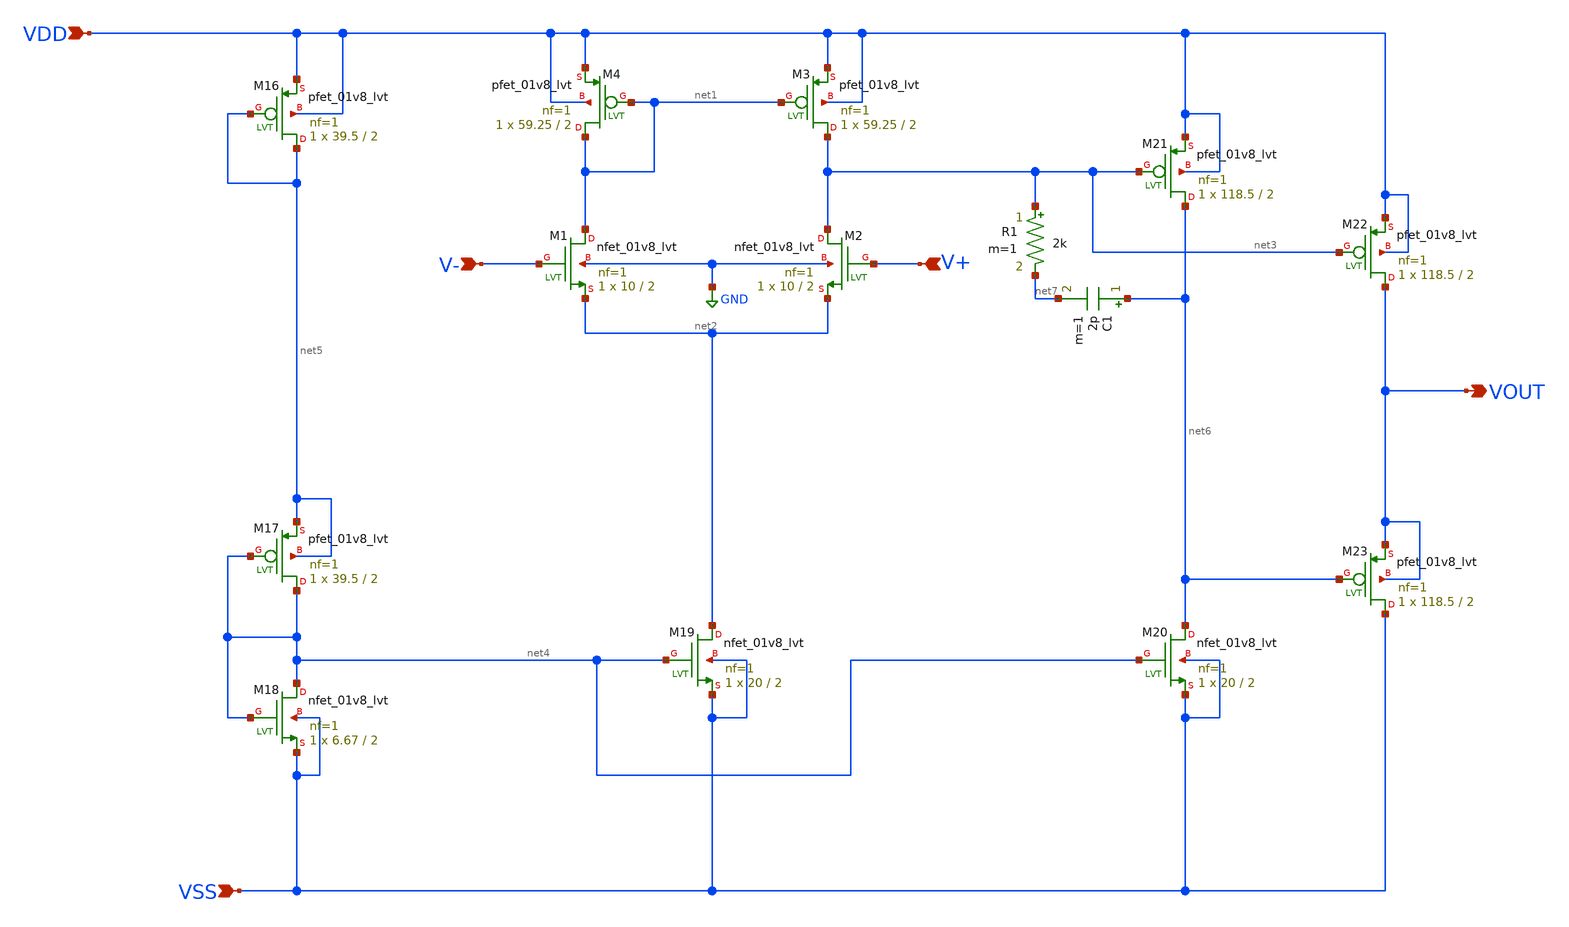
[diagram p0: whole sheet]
** sch_path: OPA.sch
**.subckt OPA VSS VOUT VDD V- V+
*.ipin VSS
*.opin VOUT
*.ipin VDD
*.ipin V-
*.ipin V+
XM16 net5 net5 VDD VDD sky130_fd_pr__pfet_01v8_lvt L=2 W=39.5 nf=1 ad='int((nf+1)/2) * W/nf * 0.29' as='int((nf+2)/2) * W/nf * 0.29'
+ pd='2*int((nf+1)/2) * (W/nf + 0.29)' ps='2*int((nf+2)/2) * (W/nf + 0.29)' nrd='0.29 / W' nrs='0.29 / W'
+ sa=0 sb=0 sd=0 mult=1 m=1
XM17 net4 net4 net5 net5 sky130_fd_pr__pfet_01v8_lvt L=2 W=39.5 nf=1 ad='int((nf+1)/2) * W/nf * 0.29'
+ as='int((nf+2)/2) * W/nf * 0.29' pd='2*int((nf+1)/2) * (W/nf + 0.29)' ps='2*int((nf+2)/2) * (W/nf + 0.29)'
+ nrd='0.29 / W' nrs='0.29 / W' sa=0 sb=0 sd=0 mult=1 m=1
XM18 net4 net4 VSS VSS sky130_fd_pr__nfet_01v8_lvt L=2 W=6.67 nf=1 ad='int((nf+1)/2) * W/nf * 0.29' as='int((nf+2)/2) * W/nf * 0.29'
+ pd='2*int((nf+1)/2) * (W/nf + 0.29)' ps='2*int((nf+2)/2) * (W/nf + 0.29)' nrd='0.29 / W' nrs='0.29 / W'
+ sa=0 sb=0 sd=0 mult=1 m=1
XM19 net2 net4 VSS VSS sky130_fd_pr__nfet_01v8_lvt L=2 W=20 nf=1 ad='int((nf+1)/2) * W/nf * 0.29' as='int((nf+2)/2) * W/nf * 0.29'
+ pd='2*int((nf+1)/2) * (W/nf + 0.29)' ps='2*int((nf+2)/2) * (W/nf + 0.29)' nrd='0.29 / W' nrs='0.29 / W'
+ sa=0 sb=0 sd=0 mult=1 m=1
XM1 net1 V- net2 GND sky130_fd_pr__nfet_01v8_lvt L=2 W=10 nf=1 ad='int((nf+1)/2) * W/nf * 0.29' as='int((nf+2)/2) * W/nf * 0.29'
+ pd='2*int((nf+1)/2) * (W/nf + 0.29)' ps='2*int((nf+2)/2) * (W/nf + 0.29)' nrd='0.29 / W' nrs='0.29 / W'
+ sa=0 sb=0 sd=0 mult=1 m=1
XM2 net3 V+ net2 GND sky130_fd_pr__nfet_01v8_lvt L=2 W=10 nf=1 ad='int((nf+1)/2) * W/nf * 0.29' as='int((nf+2)/2) * W/nf * 0.29'
+ pd='2*int((nf+1)/2) * (W/nf + 0.29)' ps='2*int((nf+2)/2) * (W/nf + 0.29)' nrd='0.29 / W' nrs='0.29 / W'
+ sa=0 sb=0 sd=0 mult=1 m=1
XM3 net3 net1 VDD VDD sky130_fd_pr__pfet_01v8_lvt L=2 W=59.25 nf=1 ad='int((nf+1)/2) * W/nf * 0.29' as='int((nf+2)/2) * W/nf * 0.29'
+ pd='2*int((nf+1)/2) * (W/nf + 0.29)' ps='2*int((nf+2)/2) * (W/nf + 0.29)' nrd='0.29 / W' nrs='0.29 / W'
+ sa=0 sb=0 sd=0 mult=1 m=1
XM4 net1 net1 VDD VDD sky130_fd_pr__pfet_01v8_lvt L=2 W=59.25 nf=1 ad='int((nf+1)/2) * W/nf * 0.29' as='int((nf+2)/2) * W/nf * 0.29'
+ pd='2*int((nf+1)/2) * (W/nf + 0.29)' ps='2*int((nf+2)/2) * (W/nf + 0.29)' nrd='0.29 / W' nrs='0.29 / W'
+ sa=0 sb=0 sd=0 mult=1 m=1
XM20 net6 net4 VSS VSS sky130_fd_pr__nfet_01v8_lvt L=2 W=20 nf=1 ad='int((nf+1)/2) * W/nf * 0.29' as='int((nf+2)/2) * W/nf * 0.29'
+ pd='2*int((nf+1)/2) * (W/nf + 0.29)' ps='2*int((nf+2)/2) * (W/nf + 0.29)' nrd='0.29 / W' nrs='0.29 / W'
+ sa=0 sb=0 sd=0 mult=1 m=1
XM21 net6 net3 VDD VDD sky130_fd_pr__pfet_01v8_lvt L=2 W=118.5 nf=1 ad='int((nf+1)/2) * W/nf * 0.29'
+ as='int((nf+2)/2) * W/nf * 0.29' pd='2*int((nf+1)/2) * (W/nf + 0.29)' ps='2*int((nf+2)/2) * (W/nf + 0.29)'
+ nrd='0.29 / W' nrs='0.29 / W' sa=0 sb=0 sd=0 mult=1 m=1
XM22 VOUT net3 VDD VDD sky130_fd_pr__pfet_01v8_lvt L=2 W=118.5 nf=1 ad='int((nf+1)/2) * W/nf * 0.29'
+ as='int((nf+2)/2) * W/nf * 0.29' pd='2*int((nf+1)/2) * (W/nf + 0.29)' ps='2*int((nf+2)/2) * (W/nf + 0.29)'
+ nrd='0.29 / W' nrs='0.29 / W' sa=0 sb=0 sd=0 mult=1 m=1
XM23 VSS net6 VOUT VOUT sky130_fd_pr__pfet_01v8_lvt L=2 W=118.5 nf=1 ad='int((nf+1)/2) * W/nf * 0.29'
+ as='int((nf+2)/2) * W/nf * 0.29' pd='2*int((nf+1)/2) * (W/nf + 0.29)' ps='2*int((nf+2)/2) * (W/nf + 0.29)'
+ nrd='0.29 / W' nrs='0.29 / W' sa=0 sb=0 sd=0 mult=1 m=1
C1 net6 net7 2p m=1
R1 net3 net7 2k m=1
**** begin user architecture code

** opencircuitdesign pdks install
.lib $::SKYWATER_MODELS/sky130.lib.spice tt

**** end user architecture code
**.ends
.GLOBAL GND
.end
